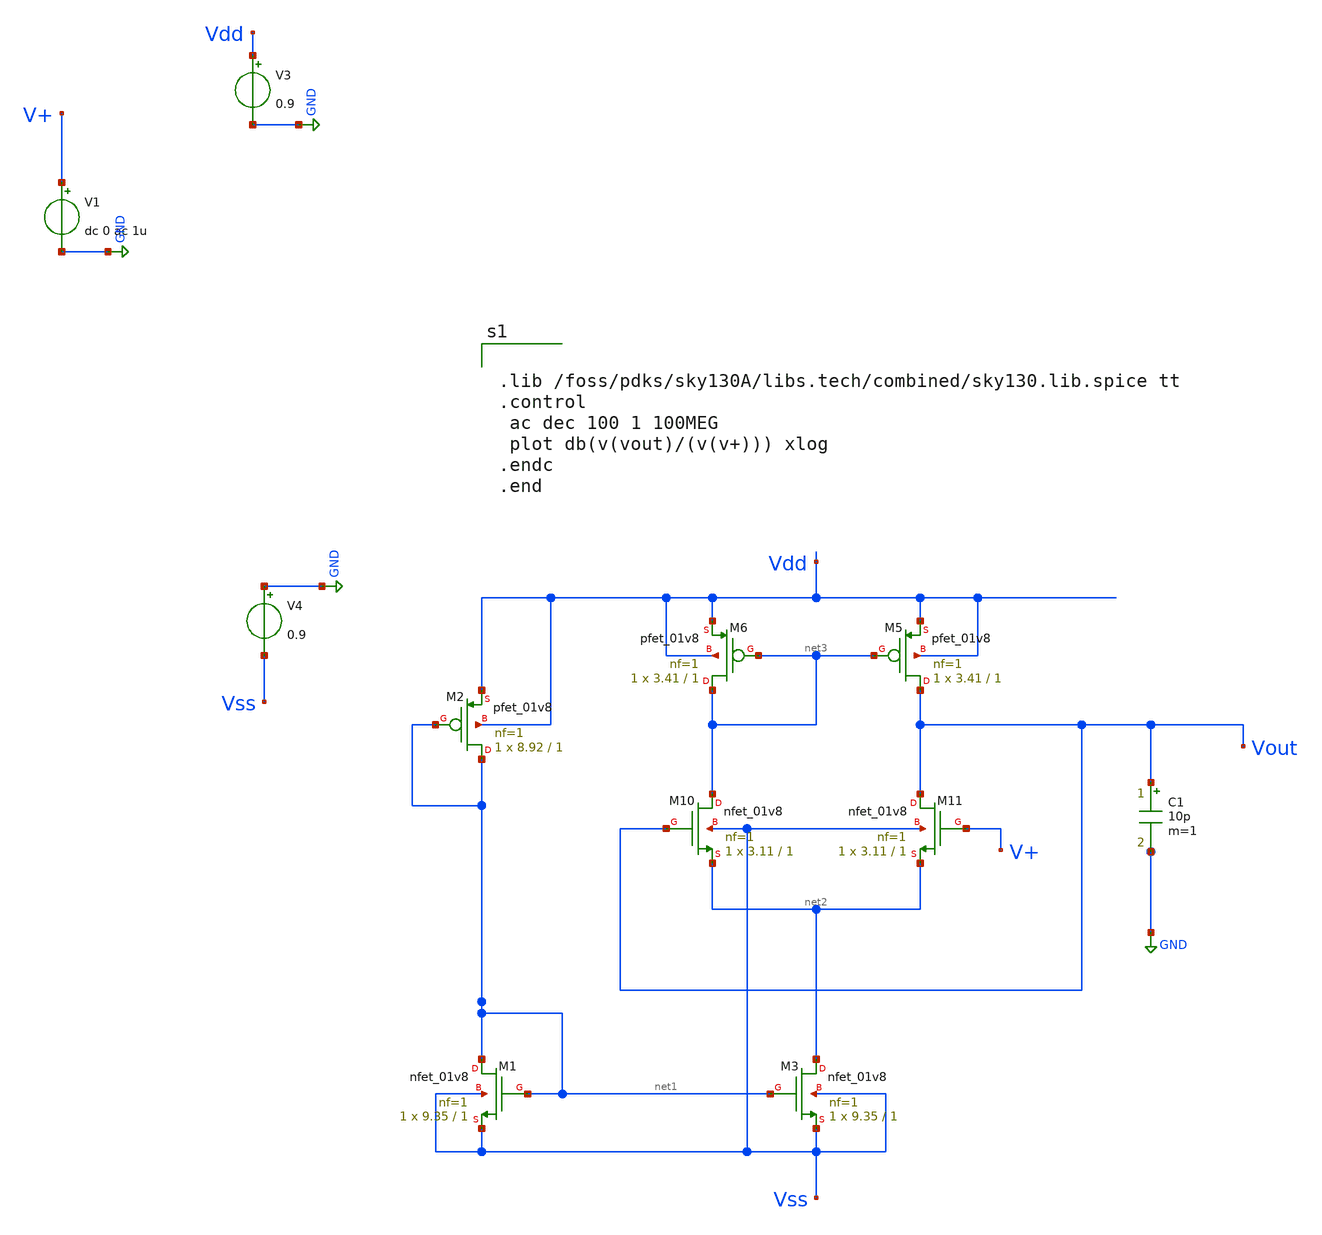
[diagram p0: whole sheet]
** sch_path: xschem/Tb_LPF.sch
**.subckt Tb_LPF
V3 Vdd GND 0.9
V4 GND Vss 0.9
V1 V+ GND dc 0 ac 1u
XM1 net1 net1 Vss Vss sky130_fd_pr__nfet_01v8 L=1 W=9.35 nf=1 ad='int((1 + 1)/2) * 9.35 / 1 * 0.29' as='int((1 + 2)/2) * 9.35 / 1 * 0.29'
+ pd='2*int((1 + 1)/2) * (9.35 / 1 + 0.29)' ps='2*int((1 + 2)/2) * (9.35 / 1 + 0.29)' nrd='0.29 / 9.35 '
+ nrs='0.29 / 9.35 ' sa=0 sb=0 sd=0 mult=1 m=1
XM3 net2 net1 Vss Vss sky130_fd_pr__nfet_01v8 L=1 W=9.35 nf=1 ad='int((1 + 1)/2) * 9.35 / 1 * 0.29' as='int((1 + 2)/2) * 9.35 / 1 * 0.29'
+ pd='2*int((1 + 1)/2) * (9.35 / 1 + 0.29)' ps='2*int((1 + 2)/2) * (9.35 / 1 + 0.29)' nrd='0.29 / 9.35 '
+ nrs='0.29 / 9.35 ' sa=0 sb=0 sd=0 mult=1 m=1
XM10 net3 Vout net2 Vss sky130_fd_pr__nfet_01v8 L=1 W=3.11 nf=1 ad='int((1 + 1)/2) * 3.11 / 1 * 0.29'
+ as='int((1 + 2)/2) * 3.11 / 1 * 0.29' pd='2*int((1 + 1)/2) * (3.11 / 1 + 0.29)' ps='2*int((1 + 2)/2) * (3.11 / 1 + 0.29)'
+ nrd='0.29 / 3.11 ' nrs='0.29 / 3.11 ' sa=0 sb=0 sd=0 mult=1 m=1
XM11 Vout V+ net2 Vss sky130_fd_pr__nfet_01v8 L=1 W=3.11 nf=1 ad='int((1 + 1)/2) * 3.11 / 1 * 0.29' as='int((1 + 2)/2) * 3.11 / 1 * 0.29'
+ pd='2*int((1 + 1)/2) * (3.11 / 1 + 0.29)' ps='2*int((1 + 2)/2) * (3.11 / 1 + 0.29)' nrd='0.29 / 3.11 '
+ nrs='0.29 / 3.11 ' sa=0 sb=0 sd=0 mult=1 m=1
XM5 Vout net3 Vdd Vdd sky130_fd_pr__pfet_01v8 L=1 W=3.41 nf=1 ad='int((1 + 1)/2) * 3.41 / 1 * 0.29' as='int((1 + 2)/2) * 3.41 / 1 * 0.29'
+ pd='2*int((1 + 1)/2) * (3.41 / 1 + 0.29)' ps='2*int((1 + 2)/2) * (3.41 / 1 + 0.29)' nrd='0.29 / 3.41 '
+ nrs='0.29 / 3.41 ' sa=0 sb=0 sd=0 mult=1 m=1
XM6 net3 net3 Vdd Vdd sky130_fd_pr__pfet_01v8 L=1 W=3.41 nf=1 ad='int((1 + 1)/2) * 3.41 / 1 * 0.29' as='int((1 + 2)/2) * 3.41 / 1 * 0.29'
+ pd='2*int((1 + 1)/2) * (3.41 / 1 + 0.29)' ps='2*int((1 + 2)/2) * (3.41 / 1 + 0.29)' nrd='0.29 / 3.41 '
+ nrs='0.29 / 3.41 ' sa=0 sb=0 sd=0 mult=1 m=1
XM2 net1 net1 Vdd Vdd sky130_fd_pr__pfet_01v8 L=1 W=8.92 nf=1 ad='int((1 + 1)/2) * 8.92 / 1 * 0.29' as='int((1 + 2)/2) * 8.92 / 1 * 0.29'
+ pd='2*int((1 + 1)/2) * (8.92 / 1 + 0.29)' ps='2*int((1 + 2)/2) * (8.92 / 1 + 0.29)' nrd='0.29 / 8.92 '
+ nrs='0.29 / 8.92 ' sa=0 sb=0 sd=0 mult=1 m=1
C1 Vout GND 10p m=1
**** begin user architecture code


.lib /foss/pdks/sky130A/libs.tech/combined/sky130.lib.spice tt
.control
 ac dec 100 1 100MEG
 plot db(v(vout)/(v(v+))) xlog
.endc
.end

**** end user architecture code
**.ends
.GLOBAL GND
.end
